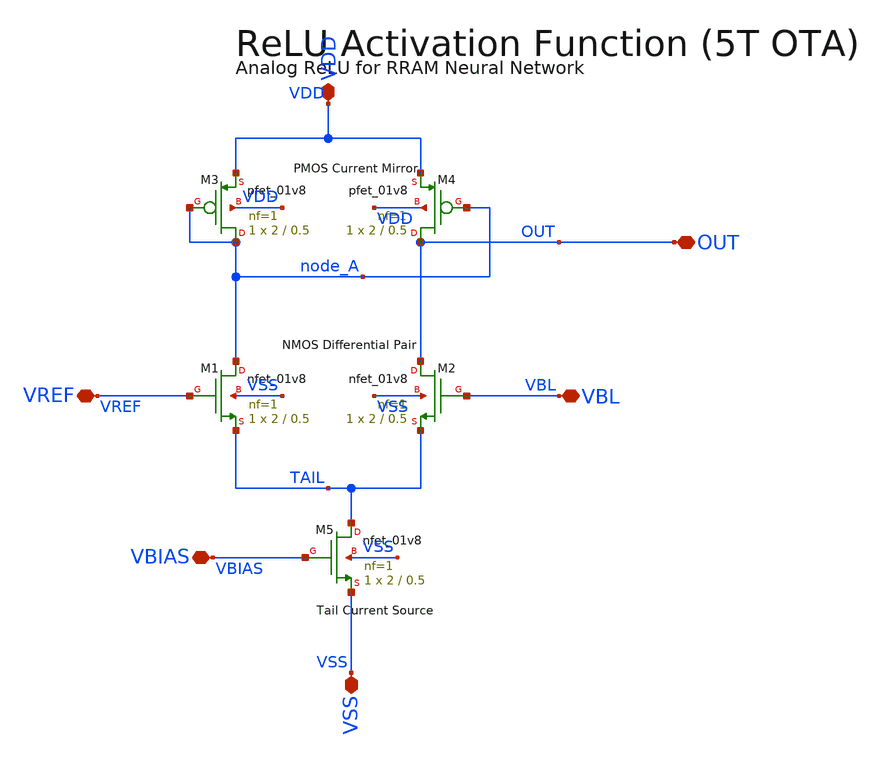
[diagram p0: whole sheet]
** sch_path: analog/xschem/xschem/relu.sch
**.subckt relu VREF VBL OUT VBIAS VDD VSS
*.iopin VREF
*.iopin VBL
*.iopin OUT
*.iopin VBIAS
*.iopin VDD
*.iopin VSS
XM3 node_A node_A VDD VDD sky130_fd_pr__pfet_01v8 L=0.5 W=2 nf=1 ad='int((nf+1)/2) * W/nf * 0.29' as='int((nf+2)/2) * W/nf * 0.29'
+ pd='2*int((nf+1)/2) * (W/nf + 0.29)' ps='2*int((nf+2)/2) * (W/nf + 0.29)' nrd='0.29 / W' nrs='0.29 / W'
+ sa=0 sb=0 sd=0 mult=1 m=1
XM4 OUT node_A VDD VDD sky130_fd_pr__pfet_01v8 L=0.5 W=2 nf=1 ad='int((nf+1)/2) * W/nf * 0.29' as='int((nf+2)/2) * W/nf * 0.29'
+ pd='2*int((nf+1)/2) * (W/nf + 0.29)' ps='2*int((nf+2)/2) * (W/nf + 0.29)' nrd='0.29 / W' nrs='0.29 / W'
+ sa=0 sb=0 sd=0 mult=1 m=1
XM1 node_A VREF TAIL VSS sky130_fd_pr__nfet_01v8 L=0.5 W=2 nf=1 ad='int((1 + 1)/2) * 2 / 1 * 0.29' as='int((1 + 2)/2) * 2 / 1 * 0.29'
+ pd='2*int((1 + 1)/2) * (2 / 1 + 0.29)' ps='2*int((1 + 2)/2) * (2 / 1 + 0.29)' nrd='0.29 / 2 ' nrs='0.29 / 2 '
+ sa=0 sb=0 sd=0 mult=1 m=1
XM2 OUT VBL TAIL VSS sky130_fd_pr__nfet_01v8 L=0.5 W=2 nf=1 ad='int((1 + 1)/2) * 2 / 1 * 0.29' as='int((1 + 2)/2) * 2 / 1 * 0.29'
+ pd='2*int((1 + 1)/2) * (2 / 1 + 0.29)' ps='2*int((1 + 2)/2) * (2 / 1 + 0.29)' nrd='0.29 / 2 ' nrs='0.29 / 2 '
+ sa=0 sb=0 sd=0 mult=1 m=1
XM5 TAIL VBIAS VSS VSS sky130_fd_pr__nfet_01v8 L=0.5 W=2 nf=1 ad='int((1 + 1)/2) * 2 / 1 * 0.29' as='int((1 + 2)/2) * 2 / 1 * 0.29'
+ pd='2*int((1 + 1)/2) * (2 / 1 + 0.29)' ps='2*int((1 + 2)/2) * (2 / 1 + 0.29)' nrd='0.29 / 2 ' nrs='0.29 / 2 '
+ sa=0 sb=0 sd=0 mult=1 m=1
**.ends
.end
